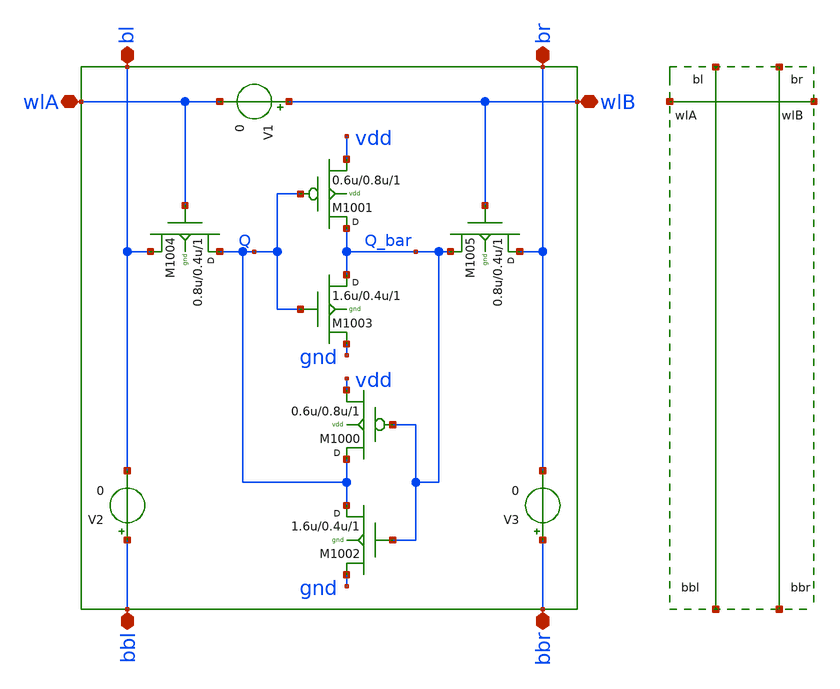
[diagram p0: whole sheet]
** sch_path: sram_2_64_scn4m_lcc/cell_1rw_passthru_sch_sym.sch
**.subckt cell_1rw_passthru_sch_sym bl br wlA wlB bbl bbr
*.iopin bl
*.iopin br
*.iopin wlA
*.iopin wlB
*.iopin bbl
*.iopin bbr
M1003 Q_bar Q gnd gnd n w=1.6u l=0.4u m=1
M1004 Q wlA bl gnd n w=0.8u l=0.4u m=1
M1001 Q_bar Q vdd vdd p w=0.6u l=0.8u m=1
M1005 br wlB Q_bar gnd n w=0.8u l=0.4u m=1
M1002 Q Q_bar gnd gnd n w=1.6u l=0.4u m=1
M1000 Q Q_bar vdd vdd p w=0.6u l=0.8u m=1
V1 wlB wlA 0
V2 bbl bl 0
V3 bbr br 0
**.ends
.end
